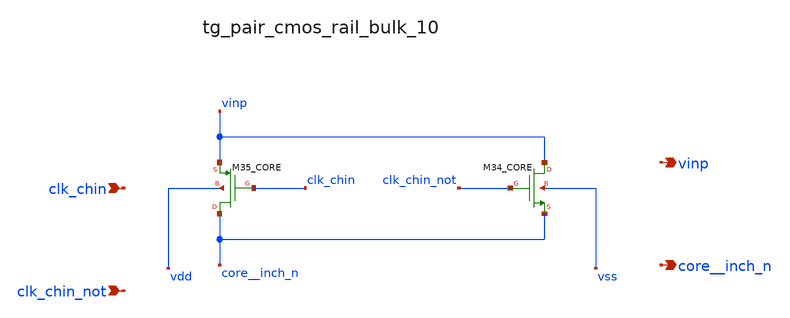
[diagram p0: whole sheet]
** sch_path: analog-db/raw/ia_006_fan_chopper_cmfb/hier/blocks/tg_pair_cmos_rail_bulk_10.sch
**.subckt tg_pair_cmos_rail_bulk_10 clk_chin clk_chin_not vinp core__inch_n
*.ipin clk_chin
*.ipin clk_chin_not
*.opin vinp
*.opin core__inch_n
XM34_CORE vinp clk_chin_not core__inch_n vss sg13_lv_nmos w=x_dut_xm34_core_w l=x_dut_xm34_core_l
+ ng=1 m=x_dut_xm34_core_m
XM35_CORE core__inch_n clk_chin vinp vdd sg13_lv_pmos w=x_dut_xm35_core_w l=x_dut_xm35_core_l ng=1
+ m=x_dut_xm35_core_m
**.ends
.end
